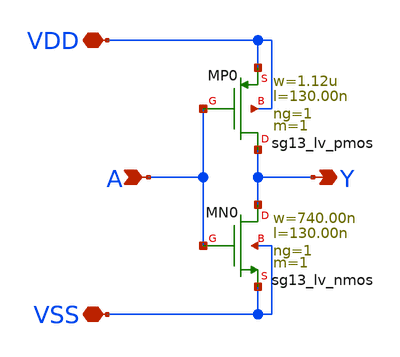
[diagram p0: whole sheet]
** sch_path: current_generator/analog/DAC/schematics/inverter.sch
**.subckt inverter Y A VDD VSS
*.opin Y
*.ipin A
*.iopin VDD
*.iopin VSS
MMN0 Y A VSS VSS sg13_lv_nmos w=740.00n l=130.00n ng=1 m=1 mm_ok=1
MMP0 Y A VDD VDD sg13_lv_pmos w=1.12u l=130.00n ng=1 m=1 mm_ok=1
**.ends
.end
